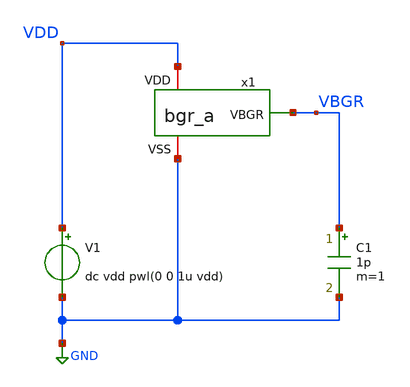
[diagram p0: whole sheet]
** sch_path: member_project/BGR/Maehashi/design/tb_bgr_a.sch
**.subckt tb_bgr_a
x1 VDD VBGR GND bgr_a
V1 VDD GND dc vdd pwl(0 0 1u vdd)
C1 VBGR GND 1p m=1
**** begin user architecture code


.option savecurrents
.temp 40
.param vthMN = 0.1 ; Slow:0.1, Fast:-0.1
.param vthMP = 0.1 ; Slow:-0.1, Fast:0.1
.param rr = 1    ; Slow:1.15, Fast:0.85, add resistor L value *rr when using this parameter
.param vdd = 5.5
.control
set units=degree
save all

*dc Vdd 4.5 5.5 0.1
*plot v(VBGR) ylimit 1.0 1.3 xlabel Vdd ylabel Vbgr
*plot @m.x1.xmp3.m1[id] xlabel Vdd ylabel Iout

dc temp 0 80 0.1
*gnuplot bgraDcVoutTemp_SF55V v(VBGR)
plot v(VBGR)  xlabel Temp ylabel Vout

.endc

 .include $::LIB/ip62_models
**** end user architecture code
**.ends
.GLOBAL GND
.end
